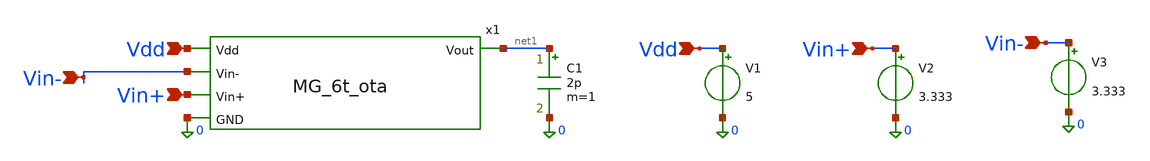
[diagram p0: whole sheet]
** sch_path: MG_6T_OTA/MG_6t_ota_testbench.sch
**.subckt MG_6t_ota_testbench Vdd Vin+ Vin- Vdd Vin+ Vin-
*.ipin Vdd
*.ipin Vin+
*.ipin Vin-
*.ipin Vdd
*.ipin Vin+
*.ipin Vin-
V1 Vdd 0 5
V2 Vin+ 0 3.333
V3 Vin- 0 3.333
C1 net1 0 2p m=1
x1 Vdd net1 Vin- Vin+ 0 MG_6t_ota
**** begin user architecture code


.include /foss/pdks/gf180mcuD/libs.tech/ngspice/design.ngspice
.lib /foss/pdks/gf180mcuD/libs.tech/ngspice/sm141064.ngspice typical
.lib /foss/pdks/gf180mcuD/libs.tech/ngspice/sm141064.ngspice res_typical
.op

**** end user architecture code
**.ends

* expanding   symbol:  MG_6t_ota.sym # of pins=5
** sym_path: MG_6T_OTA/MG_6t_ota.sym
** sch_path: MG_6T_OTA/MG_6t_ota.sch
.subckt MG_6t_ota Vdd Vout Vin- Vin+ GND
*.ipin Vdd
*.ipin Vin+
*.ipin Vin-
*.ipin GND
*.opin Vout
XM4 Vout net1 Vdd Vdd pfet_05v0 L=2u W=27u nf=14 ad='int((nf+1)/2) * W/nf * 0.18u' as='int((nf+2)/2) * W/nf * 0.18u'
+ pd='2*int((nf+1)/2) * (W/nf + 0.18u)' ps='2*int((nf+2)/2) * (W/nf + 0.18u)' nrd='0.18u / W' nrs='0.18u / W'
+ sa=0 sb=0 sd=0 m=1
XM2 Vout Vin- net2 GND nfet_05v0 L=1u W=16u nf=8 ad='int((nf+1)/2) * W/nf * 0.18u' as='int((nf+2)/2) * W/nf * 0.18u'
+ pd='2*int((nf+1)/2) * (W/nf + 0.18u)' ps='2*int((nf+2)/2) * (W/nf + 0.18u)' nrd='0.18u / W' nrs='0.18u / W'
+ sa=0 sb=0 sd=0 m=1
XM1 net1 Vin+ net2 GND nfet_05v0 L=1u W=16u nf=8 ad='int((nf+1)/2) * W/nf * 0.18u' as='int((nf+2)/2) * W/nf * 0.18u'
+ pd='2*int((nf+1)/2) * (W/nf + 0.18u)' ps='2*int((nf+2)/2) * (W/nf + 0.18u)' nrd='0.18u / W' nrs='0.18u / W'
+ sa=0 sb=0 sd=0 m=1
XM3 net1 net1 Vdd Vdd pfet_05v0 L=2u W=27u nf=14 ad='int((nf+1)/2) * W/nf * 0.18u' as='int((nf+2)/2) * W/nf * 0.18u'
+ pd='2*int((nf+1)/2) * (W/nf + 0.18u)' ps='2*int((nf+2)/2) * (W/nf + 0.18u)' nrd='0.18u / W' nrs='0.18u / W'
+ sa=0 sb=0 sd=0 m=1
XM5b net2 net4 net3 GND nfet_05v0 L=1.25u W=12u nf=8 ad='int((nf+1)/2) * W/nf * 0.18u' as='int((nf+2)/2) * W/nf * 0.18u'
+ pd='2*int((nf+1)/2) * (W/nf + 0.18u)' ps='2*int((nf+2)/2) * (W/nf + 0.18u)' nrd='0.18u / W' nrs='0.18u / W'
+ sa=0 sb=0 sd=0 m=1
XM5a net3 net5 GND GND nfet_05v0 L=1.25u W=6u nf=4 ad='int((nf+1)/2) * W/nf * 0.18u' as='int((nf+2)/2) * W/nf * 0.18u'
+ pd='2*int((nf+1)/2) * (W/nf + 0.18u)' ps='2*int((nf+2)/2) * (W/nf + 0.18u)' nrd='0.18u / W' nrs='0.18u / W'
+ sa=0 sb=0 sd=0 m=1
XR1 net4 Vdd GND ppolyf_u_3k r_width=1e-6 r_length=3e-6 m=1
XR2 net5 net4 GND ppolyf_u_3k r_width=1e-6 r_length=1e-6 m=1
XR3 GND net5 GND ppolyf_u_3k r_width=1e-6 r_length=1e-6 m=1
.ends

.end
